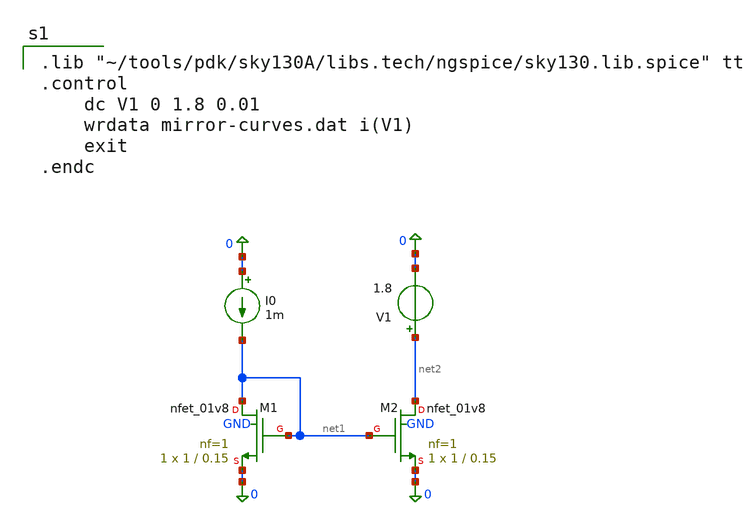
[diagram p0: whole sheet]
** sch_path: labs/current-mirror.sch
**.subckt current-mirror
XM1 net1 net1 0 GND sky130_fd_pr__nfet_01v8 L=0.15 W=1 nf=1 ad='int((nf+1)/2) * W/nf * 0.29' as='int((nf+2)/2) * W/nf * 0.29'
+ pd='2*int((nf+1)/2) * (W/nf + 0.29)' ps='2*int((nf+2)/2) * (W/nf + 0.29)' nrd='0.29 / W' nrs='0.29 / W'
+ sa=0 sb=0 sd=0 mult=1 m=1
XM2 net2 net1 0 GND sky130_fd_pr__nfet_01v8 L=0.15 W=1 nf=1 ad='int((nf+1)/2) * W/nf * 0.29' as='int((nf+2)/2) * W/nf * 0.29'
+ pd='2*int((nf+1)/2) * (W/nf + 0.29)' ps='2*int((nf+2)/2) * (W/nf + 0.29)' nrd='0.29 / W' nrs='0.29 / W'
+ sa=0 sb=0 sd=0 mult=1 m=1
I0 0 net1 1m
V1 net2 0 1.8
**** begin user architecture code

.lib "~/tools/pdk/sky130A/libs.tech/ngspice/sky130.lib.spice" tt
.control
    dc V1 0 1.8 0.01
    wrdata mirror-curves.dat i(V1)
    exit
.endc

**** end user architecture code
**.ends
.end
